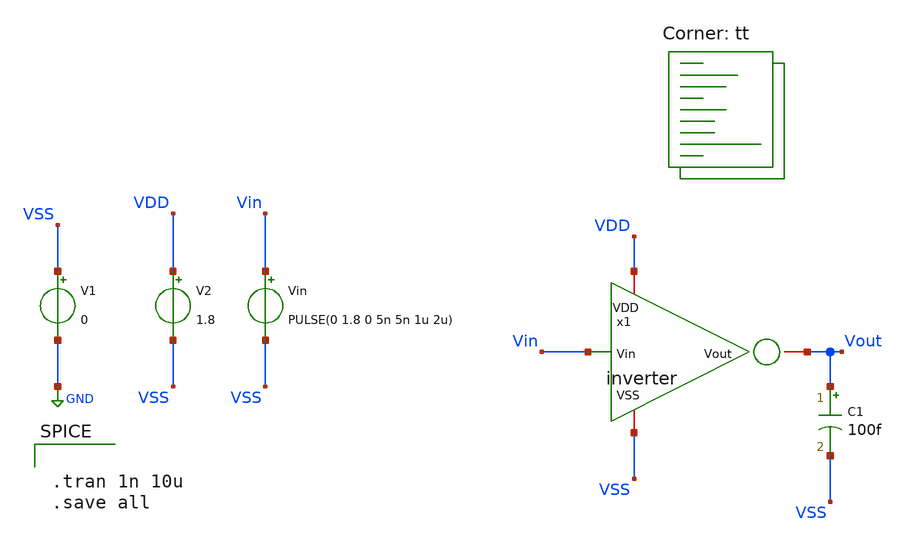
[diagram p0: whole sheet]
** sch_path: Modulo_Analogico/Lab2/inverter_tb_tran.sch
**.subckt inverter_tb_tran
x1 Vin VDD VSS Vout inverter
C1 Vout VSS 100f m=1
V1 VSS GND 0
V2 VDD VSS 1.8
Vin Vin VSS PULSE(0 1.8 0 5n 5n 1u 2u)
**** begin user architecture code


.tran 1n 10u
.save all


.lib $::SKYWATER_MODELS/sky130.lib.spice tt
**** end user architecture code
**.ends
.GLOBAL GND
.end
